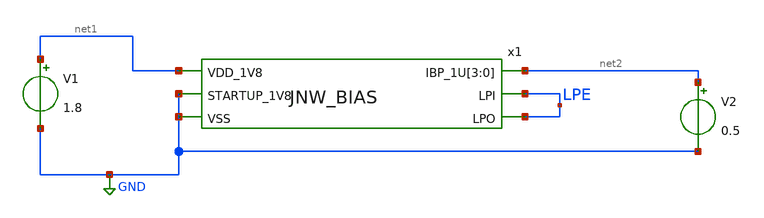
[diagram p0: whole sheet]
** sch_path: design/JNW_BIAS_SKY130A/TB_JNW_BIAS_DC.sch
**.subckt TB_JNW_BIAS_DC
x1 net1 LPE net2 net2 net2 net2 LPE GND GND JNW_BIAS
V1 net1 GND 1.8
V2 net2 GND 0.5
**** begin user architecture code



* ngspice commands
.include tb_bias_dc.spi



**** end user architecture code
**.ends
.GLOBAL GND
.end
